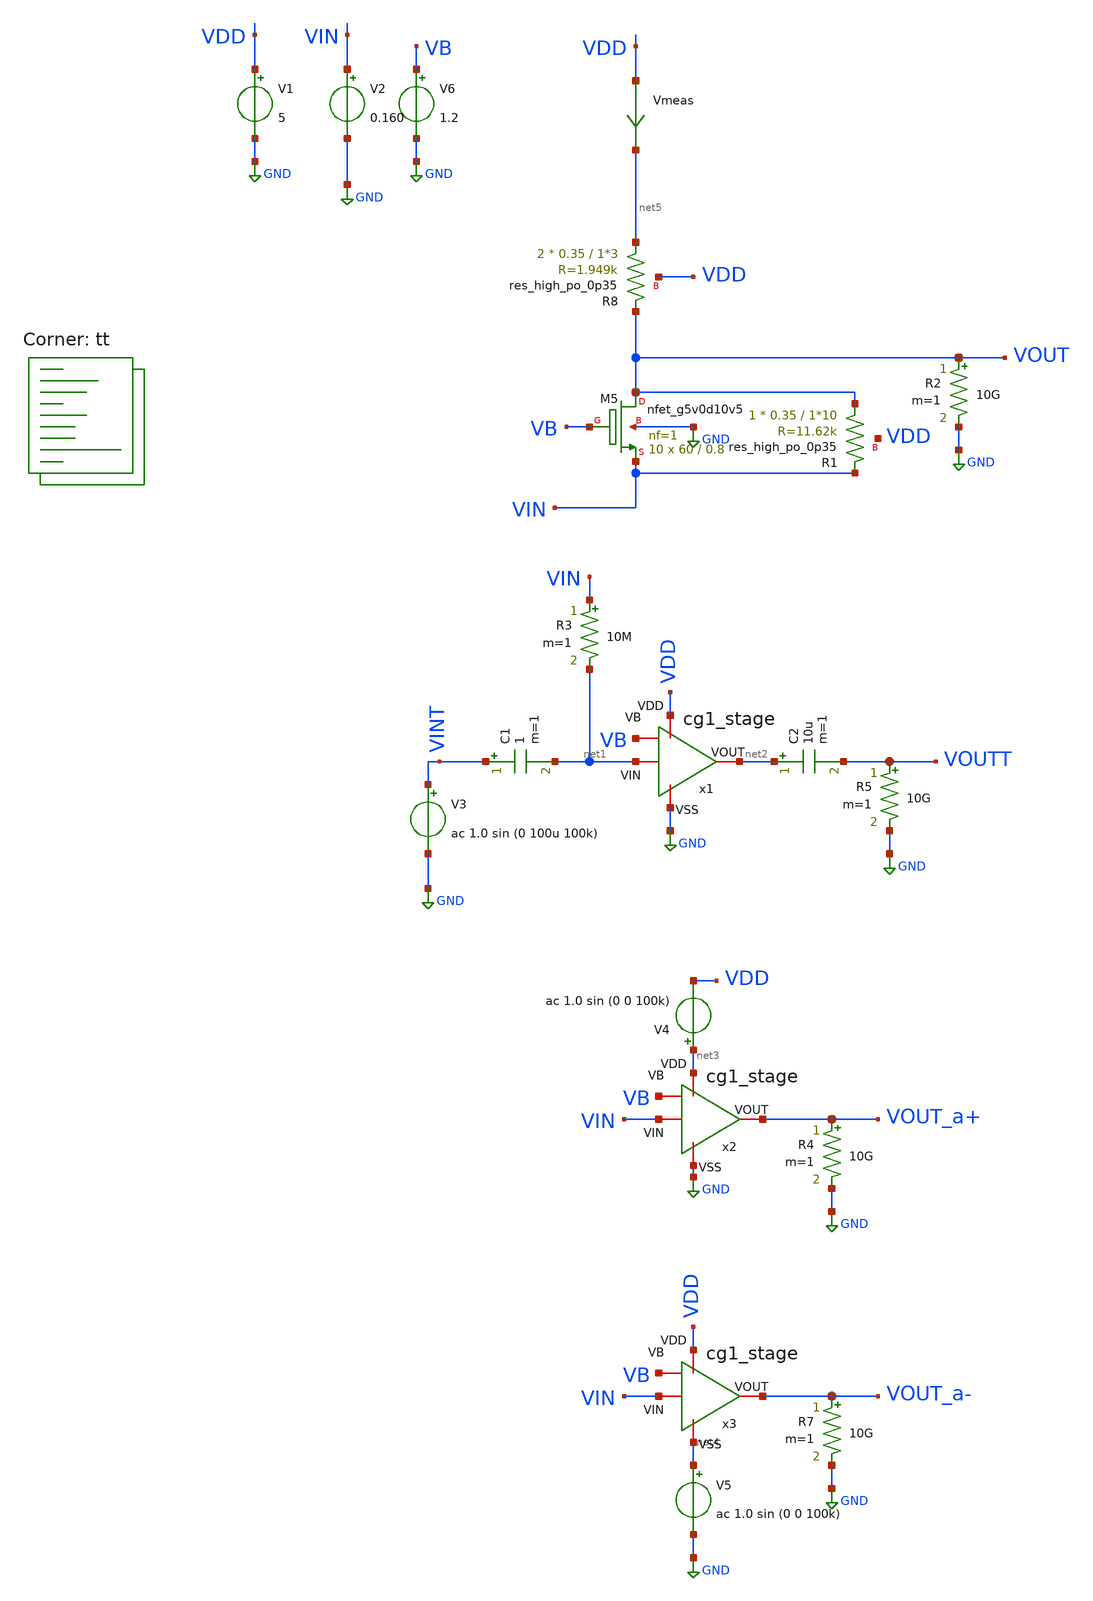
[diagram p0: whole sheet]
** sch_path: old stuff/amplifiers/single_stage_amps/stange_stages/cg_1/cg1_stage_test.sch
**.subckt cg1_stage_test
Vmeas VDD net5 0
.save i(vmeas)
V1 VDD GND 5
V2 VIN GND 0.160
V3 VINT GND ac 1.0 sin (0 100u 100k)
R2 VOUT GND 10G m=1
C1 VINT net1 1 m=1
R3 VIN net1 10M m=1
R5 VOUTT GND 10G m=1
C2 net2 VOUTT 10u m=1
R4 VOUT_a+ GND 10G m=1
V4 net3 VDD ac 1.0 sin (0 0 100k)
R7 VOUT_a- GND 10G m=1
V5 net4 GND ac 1.0 sin (0 0 100k)
XR8 net5 VOUT VDD sky130_fd_pr__res_high_po_0p35 L=1*3 mult=2 m=2
XM5 VOUT VB VIN GND sky130_fd_pr__nfet_g5v0d10v5 L=0.8 W=60 nf=1 ad='int((1 + 1)/2) * 60 / 1 * 0.29'
+ as='int((1 + 2)/2) * 60 / 1 * 0.29' pd='2*int((1 + 1)/2) * (60 / 1 + 0.29)' ps='2*int((1 + 2)/2) * (60 / 1 + 0.29)'
+ nrd='0.29 / 60 ' nrs='0.29 / 60 ' sa=0 sb=0 sd=0 mult=10 m=10
V6 VB GND 1.2
XR1 VOUT VIN VDD sky130_fd_pr__res_high_po_0p35 L=1*10 mult=1 m=1
x1 VDD GND net1 net2 VB cg1_stage
x2 net3 GND VIN VOUT_a+ VB cg1_stage
x3 VDD net4 VIN VOUT_a- VB cg1_stage
**** begin user architecture code

**************************************************************
**************************************************************
**************************************************************
**************************************************************
**************************************************************
*LIBs*********************************************************
**************************************************************
**************************************************************
**************************************************************
**************************************************************
**************************************************************
*.lib $::SKYWATER_MODELS/sky130.lib.spice tt
* chose the corners in the corner file
* tt_mm for mismatch
* ss ff sf fs standart corners
* ll hh lh hl capacitor and resistors corners
* mc for total process variation including corners
**************************************************************
**************************************************************
**************************************************************
**************************************************************
**************************************************************
*Corners/montecarlo options***********************************
**************************************************************
**************************************************************
**************************************************************
**************************************************************
**************************************************************
.TEMP 27
**************************************************************
**************************************************************
**************************************************************
**************************************************************
*SIMULATION and Plots*****************************************
**************************************************************
**************************************************************
**************************************************************
**************************************************************
.control
save all
dc V2 0 5 0.01
*dc simulation
plot v(VOUT) v(VIN) deriv(v(VOUT))
*ploting VIN VOUT and the voltage gain
plot i(Vmeas)
*ploting the current for curiosity
tran 0.1ns 20u
*transient simulation
plot (v(VINT)) (v(VOUTT))
*simple plot to exemplify the gain
fft v(VOUTT) v(VINT)
*fast fourier transfor
plot mag(v(VOUTT)) mag(v(VINT))
* analyse the frequency spectrum of the transient waves, to detect distortion
ac dec 20 1 50G
*simple ac simulation
plot db(v(VOUTT))
plot db(v(VOUT_a+))
plot db(v(VOUT_a-))
*gain in function of the input frequency
.endc

.lib $::SKYWATER_MODELS/sky130.lib.spice tt
**** end user architecture code
**.ends
.GLOBAL GND
.end
